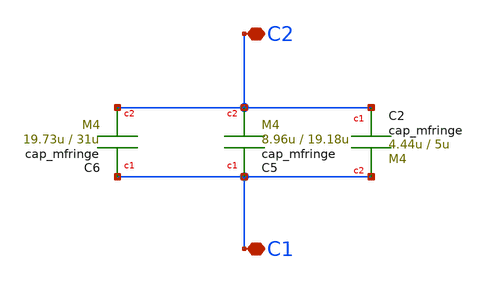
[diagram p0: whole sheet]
** sch_path: cfringe33x55.sch
**.subckt cfringe33x55 C2 C1
*.iopin C2
*.iopin C1
XC2 C2 C1 cap_mfringe w=4.44u l=5u mmin=1 mmax=4
XC5 C1 C2 cap_mfringe w=8.96u l=19.18u mmin=1 mmax=4
XC6 C1 C2 cap_mfringe w=19.73u l=31u mmin=1 mmax=4
**.ends
.end
